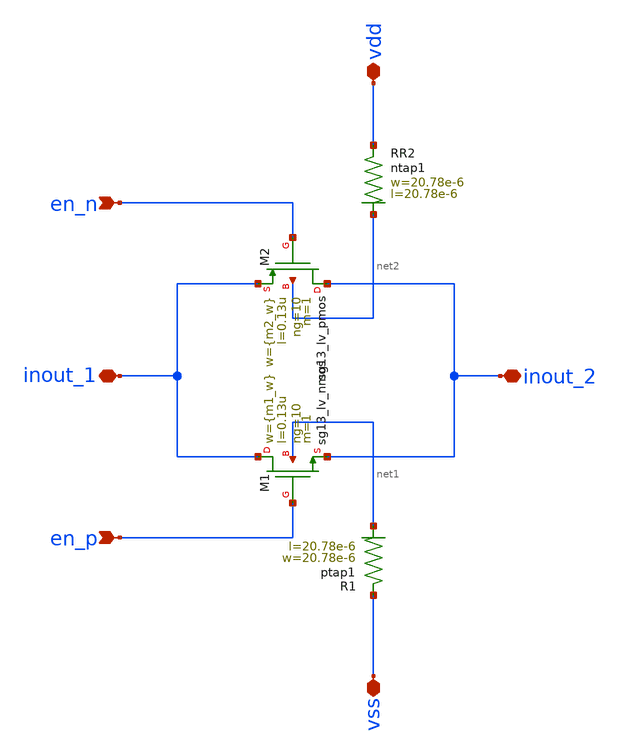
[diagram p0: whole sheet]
** sch_path: design_data/xschem/transmission_gate_lv.sch
**.subckt transmission_gate_lv inout_1 inout_2 en_p vdd vss en_n
*.iopin inout_1
*.iopin inout_2
*.ipin en_p
*.iopin vdd
*.iopin vss
*.ipin en_n
XR1 vss net1 ptap1 R=1.903 w=20.78e-6 l=20.78e-6
XR2 vdd net2 ntap1 R=1.903 w=20.78e-6 l=20.78e-6
XM2 inout_2 en_n inout_1 net2 sg13_lv_pmos w={m2_w} l=0.13u ng=10 m=1 mm_ok=1
XM1 inout_1 en_p inout_2 net1 sg13_lv_nmos w={m1_w} l=0.13u ng=10 m=1 mm_ok=1
**.ends
.end
